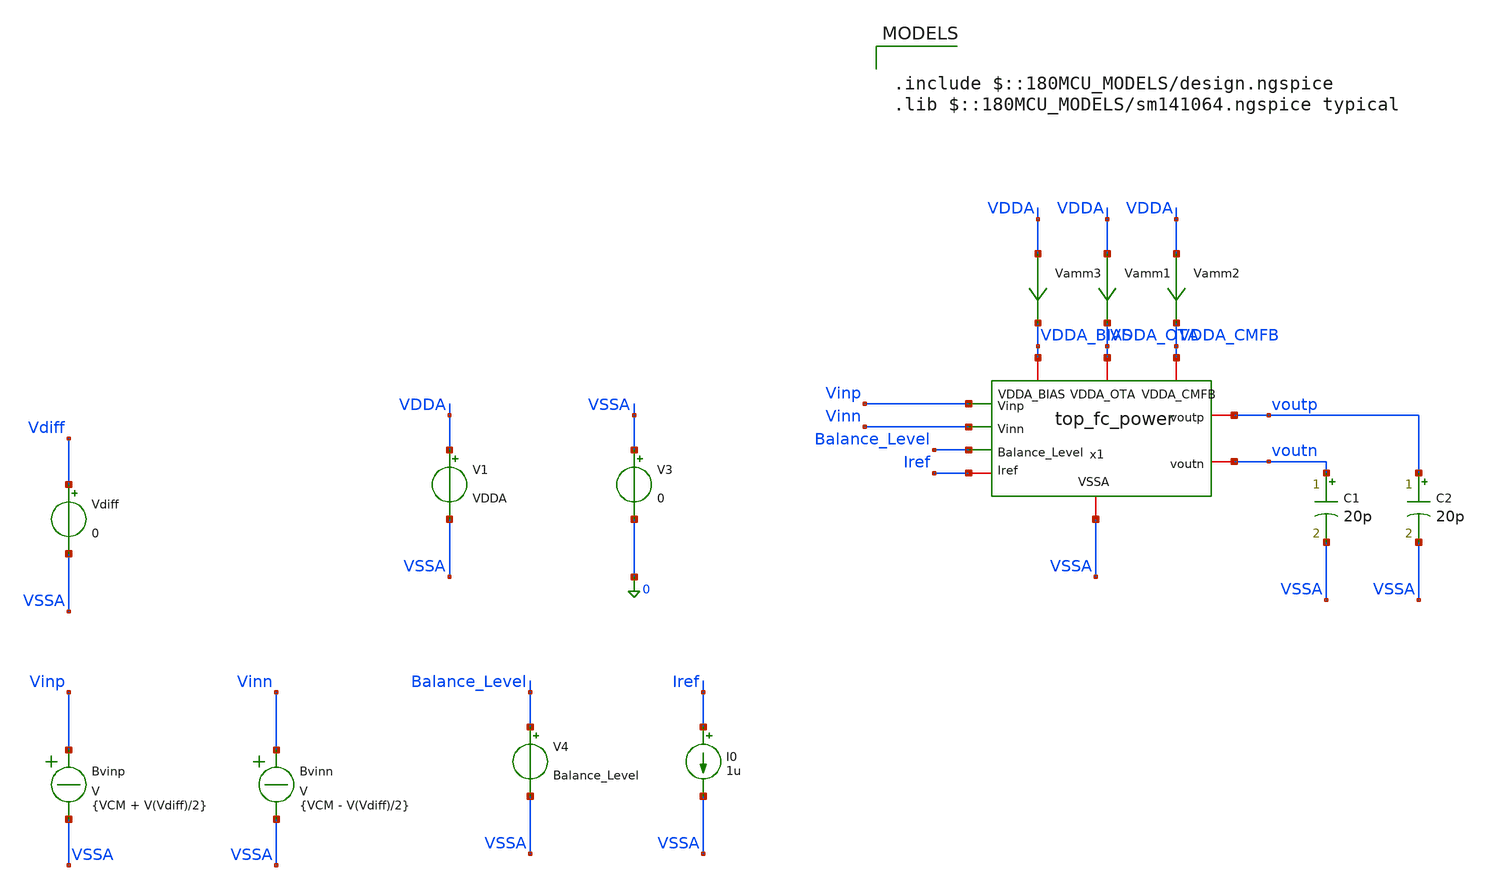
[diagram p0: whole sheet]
** sch_path: Folded_cascode/testbenches/top_fc_power_tb.sch
**.subckt top_fc_power_tb
C1 voutn VSSA 20p m=1
C2 voutp VSSA 20p m=1
V1 VDDA VSSA VDDA
V3 VSSA 0 0
V4 Balance_Level VSSA Balance_Level
I0 Iref VSSA 1u
Bvinp Vinp VSSA V = {VCM + V(Vdiff)/2}
Bvinn Vinn VSSA V = {VCM - V(Vdiff)/2}
Vdiff Vdiff VSSA 0
x1 VDDA_BIAS VDDA_OTA VDDA_CMFB Balance_Level Vinp voutp voutn Vinn Iref VSSA top_fc_power
Vamm1 VDDA VDDA_OTA 0
.save i(vamm1)
Vamm2 VDDA VDDA_CMFB 0
.save i(vamm2)
Vamm3 VDDA VDDA_BIAS 0
.save i(vamm3)
**** begin user architecture code

.include $::180MCU_MODELS/design.ngspice
.lib $::180MCU_MODELS/sm141064.ngspice typical



.temp 27
.param VDDA = 5
.param Balance_Level = 1.5
.param VD = 0
.param VCM = 2.5
.param sw_stat_global=0
.param sw_stat_mismatch=0

.control
option sparse
set filetype=ascii
set wr_singlescale
set wr_vecnames
save all
save @m.x1.x1.xm1.m0[id]
save @m.x1.x1.xm1.m0[gm]
save @m.x1.x1.xm1.m0[vgs]
save @m.x1.x1.xm1.m0[vds]
save @m.x1.x1.xm1.m0[vth]
save @m.x1.x1.xm1.m0[gds]
save @m.x1.x1.xm1.m0[vdsat]

save @m.x1.x1.xm2.m0[id]
save @m.x1.x1.xm2.m0[gm]
save @m.x1.x1.xm2.m0[vgs]
save @m.x1.x1.xm2.m0[vds]
save @m.x1.x1.xm2.m0[vth]
save @m.x1.x1.xm2.m0[gds]
save @m.x1.x1.xm2.m0[vdsat]

save @m.x1.x1.xm9.m0[id]
save @m.x1.x1.xm9.m0[gm]
save @m.x1.x1.xm9.m0[vgs]
save @m.x1.x1.xm9.m0[vds]
save @m.x1.x1.xm9.m0[vth]
save @m.x1.x1.xm9.m0[gds]
save @m.x1.x1.xm9.m0[vdsat]

save @m.x1.x1.xm8.m0[id]
save @m.x1.x1.xm8.m0[gm]
save @m.x1.x1.xm8.m0[vgs]
save @m.x1.x1.xm8.m0[vds]
save @m.x1.x1.xm8.m0[vth]
save @m.x1.x1.xm8.m0[gds]
save @m.x1.x1.xm8.m0[vdsat]

save @m.x1.x1.xm6.m0[id]
save @m.x1.x1.xm6.m0[gm]
save @m.x1.x1.xm6.m0[vgs]
save @m.x1.x1.xm6.m0[vds]
save @m.x1.x1.xm6.m0[vth]
save @m.x1.x1.xm6.m0[gds]
save @m.x1.x1.xm6.m0[vdsat]

save @m.x1.x1.xm5.m0[id]
save @m.x1.x1.xm5.m0[gm]
save @m.x1.x1.xm5.m0[vgs]
save @m.x1.x1.xm5.m0[vds]
save @m.x1.x1.xm5.m0[vth]
save @m.x1.x1.xm5.m0[gds]
save @m.x1.x1.xm5.m0[vdsat]

save @m.x1.x2.xm1.m0[id]
save @m.x1.x2.xm1.m0[gm]
save @m.x1.x2.xm1.m0[vgs]
save @m.x1.x2.xm1.m0[vds]
save @m.x1.x2.xm1.m0[vth]
save @m.x1.x2.xm1.m0[gds]

save @m.x1.x2.xm2.m0[id]
save @m.x1.x2.xm2.m0[gm]
save @m.x1.x2.xm2.m0[vgs]
save @m.x1.x2.xm2.m0[vds]
save @m.x1.x2.xm2.m0[vth]
save @m.x1.x2.xm2.m0[gds]

save @m.x1.x2.xm3.m0[id]
save @m.x1.x2.xm3.m0[gm]
save @m.x1.x2.xm3.m0[vgs]
save @m.x1.x2.xm3.m0[vds]
save @m.x1.x2.xm3.m0[vth]
save @m.x1.x2.xm3.m0[gds]

save @m.x1.x2.xm4.m0[id]
save @m.x1.x2.xm4.m0[gm]
save @m.x1.x2.xm4.m0[vgs]
save @m.x1.x2.xm4.m0[vds]
save @m.x1.x2.xm4.m0[vth]
save @m.x1.x2.xm4.m0[gds]

save @m.x1.x2.xm5.m0[id]
save @m.x1.x2.xm5.m0[gm]
save @m.x1.x2.xm5.m0[vgs]
save @m.x1.x2.xm5.m0[vds]
save @m.x1.x2.xm5.m0[vth]
save @m.x1.x2.xm5.m0[gds]

save @m.x1.x2.xm6.m0[id]
save @m.x1.x2.xm6.m0[gm]
save @m.x1.x2.xm6.m0[vgs]
save @m.x1.x2.xm6.m0[vds]
save @m.x1.x2.xm6.m0[vth]
save @m.x1.x2.xm6.m0[gds]

save @m.x1.x2.xm7.m0[id]
save @m.x1.x2.xm7.m0[gm]
save @m.x1.x2.xm7.m0[vgs]
save @m.x1.x2.xm7.m0[vds]
save @m.x1.x2.xm7.m0[vth]
save @m.x1.x2.xm7.m0[gds]

save @m.x1.x2.xm8.m0[id]
save @m.x1.x2.xm8.m0[gm]
save @m.x1.x2.xm8.m0[vgs]
save @m.x1.x2.xm8.m0[vds]
save @m.x1.x2.xm8.m0[vth]
save @m.x1.x2.xm8.m0[gds]

save @m.x1.x2.xm9.m0[id]
save @m.x1.x2.xm9.m0[gm]
save @m.x1.x2.xm9.m0[vgs]
save @m.x1.x2.xm9.m0[vds]
save @m.x1.x2.xm9.m0[vth]
save @m.x1.x2.xm9.m0[gds]

save @m.x1.x3.xm1.m0[id]
save @m.x1.x3.xm1.m0[gm]
save @m.x1.x3.xm1.m0[vgs]
save @m.x1.x3.xm1.m0[vds]
save @m.x1.x3.xm1.m0[vth]
save @m.x1.x3.xm1.m0[gds]

save @m.x1.x3.xm2.m0[id]
save @m.x1.x3.xm2.m0[gm]
save @m.x1.x3.xm2.m0[vgs]
save @m.x1.x3.xm2.m0[vds]
save @m.x1.x3.xm2.m0[vth]
save @m.x1.x3.xm2.m0[gds]

save @m.x1.x3.xm3.m0[id]
save @m.x1.x3.xm3.m0[gm]
save @m.x1.x3.xm3.m0[vgs]
save @m.x1.x3.xm3.m0[vds]
save @m.x1.x3.xm3.m0[vth]
save @m.x1.x3.xm3.m0[gds]

save @m.x1.x3.xm4.m0[id]
save @m.x1.x3.xm4.m0[gm]
save @m.x1.x3.xm4.m0[vgs]
save @m.x1.x3.xm4.m0[vds]
save @m.x1.x3.xm4.m0[vth]
save @m.x1.x3.xm4.m0[gds]

save @m.x1.x3.xm5.m0[id]
save @m.x1.x3.xm5.m0[gm]
save @m.x1.x3.xm5.m0[vgs]
save @m.x1.x3.xm5.m0[vds]
save @m.x1.x3.xm5.m0[vth]
save @m.x1.x3.xm5.m0[gds]

save @m.x1.x3.xm6.m0[id]
save @m.x1.x3.xm6.m0[gm]
save @m.x1.x3.xm6.m0[vgs]
save @m.x1.x3.xm6.m0[vds]
save @m.x1.x3.xm6.m0[vth]
save @m.x1.x3.xm6.m0[gds]

save @m.x1.x3.xm7.m0[id]
save @m.x1.x3.xm7.m0[gm]
save @m.x1.x3.xm7.m0[vgs]
save @m.x1.x3.xm7.m0[vds]
save @m.x1.x3.xm7.m0[vth]
save @m.x1.x3.xm7.m0[gds]

save @m.x1.x3.xm8.m0[id]
save @m.x1.x3.xm8.m0[gm]
save @m.x1.x3.xm8.m0[vgs]
save @m.x1.x3.xm8.m0[vds]
save @m.x1.x3.xm8.m0[vth]
save @m.x1.x3.xm8.m0[gds]

save @m.x1.x3.xm9.m0[id]
save @m.x1.x3.xm9.m0[gm]
save @m.x1.x3.xm9.m0[vgs]
save @m.x1.x3.xm9.m0[vds]
save @m.x1.x3.xm9.m0[vth]
save @m.x1.x3.xm9.m0[gds]

save @m.x1.x3.xm10.m0[id]
save @m.x1.x3.xm10.m0[gm]
save @m.x1.x3.xm10.m0[vgs]
save @m.x1.x3.xm10.m0[vds]
save @m.x1.x3.xm10.m0[vth]
save @m.x1.x3.xm10.m0[gds]

save @m.x1.x3.xm11.m0[id]
save @m.x1.x3.xm11.m0[gm]
save @m.x1.x3.xm11.m0[vgs]
save @m.x1.x3.xm11.m0[vds]
save @m.x1.x3.xm11.m0[vth]
save @m.x1.x3.xm11.m0[gds]

save @m.x1.x3.xm12.m0[id]
save @m.x1.x3.xm12.m0[gm]
save @m.x1.x3.xm12.m0[vgs]
save @m.x1.x3.xm12.m0[vds]
save @m.x1.x3.xm12.m0[vth]
save @m.x1.x3.xm12.m0[gds]

save @m.x1.x3.xm13.m0[id]
save @m.x1.x3.xm13.m0[gm]
save @m.x1.x3.xm13.m0[vgs]
save @m.x1.x3.xm13.m0[vds]
save @m.x1.x3.xm13.m0[vth]
save @m.x1.x3.xm13.m0[gds]

save @m.x1.x3.xm14.m0[id]
save @m.x1.x3.xm14.m0[gm]
save @m.x1.x3.xm14.m0[vgs]
save @m.x1.x3.xm14.m0[vds]
save @m.x1.x3.xm14.m0[vth]
save @m.x1.x3.xm14.m0[gds]

save @m.x1.x3.xm15.m0[id]
save @m.x1.x3.xm15.m0[gm]
save @m.x1.x3.xm15.m0[vgs]
save @m.x1.x3.xm15.m0[vds]
save @m.x1.x3.xm15.m0[vth]
save @m.x1.x3.xm15.m0[gds]

save @m.x1.x3.xm16.m0[id]
save @m.x1.x3.xm16.m0[gm]
save @m.x1.x3.xm16.m0[vgs]
save @m.x1.x3.xm16.m0[vds]
save @m.x1.x3.xm16.m0[vth]
save @m.x1.x3.xm16.m0[gds]

save @m.x1.x3.xm17.m0[id]
save @m.x1.x3.xm17.m0[gm]
save @m.x1.x3.xm17.m0[vgs]
save @m.x1.x3.xm17.m0[vds]
save @m.x1.x3.xm17.m0[vth]
save @m.x1.x3.xm17.m0[gds]

save @m.x1.x3.xm18.m0[id]
save @m.x1.x3.xm18.m0[gm]
save @m.x1.x3.xm18.m0[vgs]
save @m.x1.x3.xm18.m0[vds]
save @m.x1.x3.xm18.m0[vth]
save @m.x1.x3.xm18.m0[gds]

save @m.x1.x3.xm21.m0[id]
save @m.x1.x3.xm21.m0[gm]
save @m.x1.x3.xm21.m0[vgs]
save @m.x1.x3.xm21.m0[vds]
save @m.x1.x3.xm21.m0[vth]
save @m.x1.x3.xm21.m0[gds]

save @m.x1.x3.xm22.m0[id]
save @m.x1.x3.xm22.m0[gm]
save @m.x1.x3.xm22.m0[vgs]
save @m.x1.x3.xm22.m0[vds]
save @m.x1.x3.xm22.m0[vth]
save @m.x1.x3.xm22.m0[gds]

op
write top_fc_op_tb.raw all

* ============================================================
* SUPPLY CURRENTS
*
* Current through voltage sources follows the SPICE sign
* convention. abs() is used so that power consumption is
* reported as a positive value.
* ============================================================

let i_ota  = abs(i(Vamm1))
let i_cmfb = abs(i(Vamm2))
let i_bias = abs(i(Vamm3))

let i_total = i_ota + i_cmfb + i_bias


* ============================================================
* DC POWER
*
* VDDA = 5 V nominal
* ============================================================

let p_ota  = VDDA * i_ota
let p_cmfb = VDDA * i_cmfb
let p_bias = VDDA * i_bias

let p_total = p_ota + p_cmfb + p_bias


* ============================================================
* UNIT CONVERSION
* ============================================================

let i_ota_uA   = i_ota * 1e6
let i_cmfb_uA  = i_cmfb * 1e6
let i_bias_uA  = i_bias * 1e6

let i_total_uA = i_total * 1e6

let p_ota_mW   = p_ota * 1e3
let p_cmfb_mW  = p_cmfb * 1e3
let p_bias_mW  = p_bias * 1e3

let p_total_mW = p_total * 1e3


* ============================================================
* POWER DISTRIBUTION
* ============================================================

let ota_power_percent  = 100 * p_ota  / p_total
let cmfb_power_percent = 100 * p_cmfb / p_total
let bias_power_percent = 100 * p_bias / p_total


* ============================================================
* PRINT RESULTS
* ============================================================

echo
echo ==========================================
echo DC POWER CONSUMPTION
echo ==========================================

print i_ota_uA
print i_cmfb_uA
print i_bias_uA
print i_total_uA

print p_ota_mW
print p_cmfb_mW
print p_bias_mW
print p_total_mW

print ota_power_percent
print cmfb_power_percent
print bias_power_percent

* ============================================================
* OPTIONAL SANITY CHECK
*
* Total current drawn from the main VDDA source should be
* approximately equal to:
*
*     I_OTA + I_CMFB + I_BIAS
* ============================================================

let i_vdda = abs(i(V1))
let i_vdda_uA = i_vdda * 1e6

print i_vdda_uA


* ============================================================
* SAVE OPERATING POINT
* ============================================================

write top_fc_power_tb.raw

.endc


**** end user architecture code
**.ends
.end
